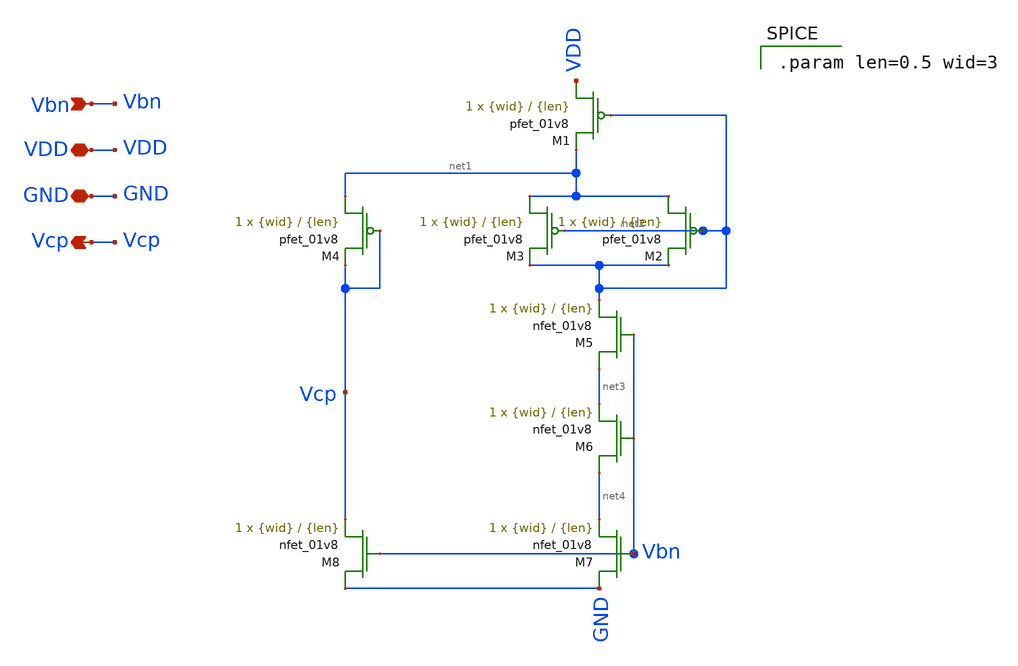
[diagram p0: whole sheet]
** sch_path: final/schematics/cascode_bias_pmos.sch
**.subckt cascode_bias_pmos Vbn VDD GND Vcp
*.ipin Vbn
*.iopin VDD
*.iopin GND
*.opin Vcp
XM1 VDD net2 net1 VDD sky130_fd_pr__pfet_01v8 L={len} W={wid} nf=1 ad='int((nf+1)/2) * W/nf * 0.29' as='int((nf+2)/2) * W/nf * 0.29'
+ pd='2*int((nf+1)/2) * (W/nf + 0.29)' ps='2*int((nf+2)/2) * (W/nf + 0.29)' nrd='0.29 / W' nrs='0.29 / W'
+ sa=0 sb=0 sd=0 mult=1 m=1
XM2 net1 net2 net2 VDD sky130_fd_pr__pfet_01v8 L={len} W={wid} nf=1 ad='int((nf+1)/2) * W/nf * 0.29'
+ as='int((nf+2)/2) * W/nf * 0.29' pd='2*int((nf+1)/2) * (W/nf + 0.29)' ps='2*int((nf+2)/2) * (W/nf + 0.29)'
+ nrd='0.29 / W' nrs='0.29 / W' sa=0 sb=0 sd=0 mult=1 m=1
XM3 net1 net2 net2 VDD sky130_fd_pr__pfet_01v8 L={len} W={wid} nf=1 ad='int((nf+1)/2) * W/nf * 0.29'
+ as='int((nf+2)/2) * W/nf * 0.29' pd='2*int((nf+1)/2) * (W/nf + 0.29)' ps='2*int((nf+2)/2) * (W/nf + 0.29)'
+ nrd='0.29 / W' nrs='0.29 / W' sa=0 sb=0 sd=0 mult=1 m=1
XM4 net1 Vcp Vcp VDD sky130_fd_pr__pfet_01v8 L={len} W={wid} nf=1 ad='int((nf+1)/2) * W/nf * 0.29' as='int((nf+2)/2) * W/nf * 0.29'
+ pd='2*int((nf+1)/2) * (W/nf + 0.29)' ps='2*int((nf+2)/2) * (W/nf + 0.29)' nrd='0.29 / W' nrs='0.29 / W'
+ sa=0 sb=0 sd=0 mult=1 m=1
XM5 net3 Vbn net2 GND sky130_fd_pr__nfet_01v8 L={len} W={wid} nf=1 ad='int((nf+1)/2) * W/nf * 0.29' as='int((nf+2)/2) * W/nf * 0.29'
+ pd='2*int((nf+1)/2) * (W/nf + 0.29)' ps='2*int((nf+2)/2) * (W/nf + 0.29)' nrd='0.29 / W' nrs='0.29 / W'
+ sa=0 sb=0 sd=0 mult=1 m=1
XM6 net4 Vbn net3 GND sky130_fd_pr__nfet_01v8 L={len} W={wid} nf=1 ad='int((nf+1)/2) * W/nf * 0.29' as='int((nf+2)/2) * W/nf * 0.29'
+ pd='2*int((nf+1)/2) * (W/nf + 0.29)' ps='2*int((nf+2)/2) * (W/nf + 0.29)' nrd='0.29 / W' nrs='0.29 / W'
+ sa=0 sb=0 sd=0 mult=1 m=1
XM7 GND Vbn net4 GND sky130_fd_pr__nfet_01v8 L={len} W={wid} nf=1 ad='int((nf+1)/2) * W/nf * 0.29' as='int((nf+2)/2) * W/nf * 0.29'
+ pd='2*int((nf+1)/2) * (W/nf + 0.29)' ps='2*int((nf+2)/2) * (W/nf + 0.29)' nrd='0.29 / W' nrs='0.29 / W'
+ sa=0 sb=0 sd=0 mult=1 m=1
XM8 GND Vbn Vcp GND sky130_fd_pr__nfet_01v8 L={len} W={wid} nf=1 ad='int((nf+1)/2) * W/nf * 0.29' as='int((nf+2)/2) * W/nf * 0.29'
+ pd='2*int((nf+1)/2) * (W/nf + 0.29)' ps='2*int((nf+2)/2) * (W/nf + 0.29)' nrd='0.29 / W' nrs='0.29 / W'
+ sa=0 sb=0 sd=0 mult=1 m=1
**** begin user architecture code

.param len=0.5 wid=3

**** end user architecture code
**.ends
.end
